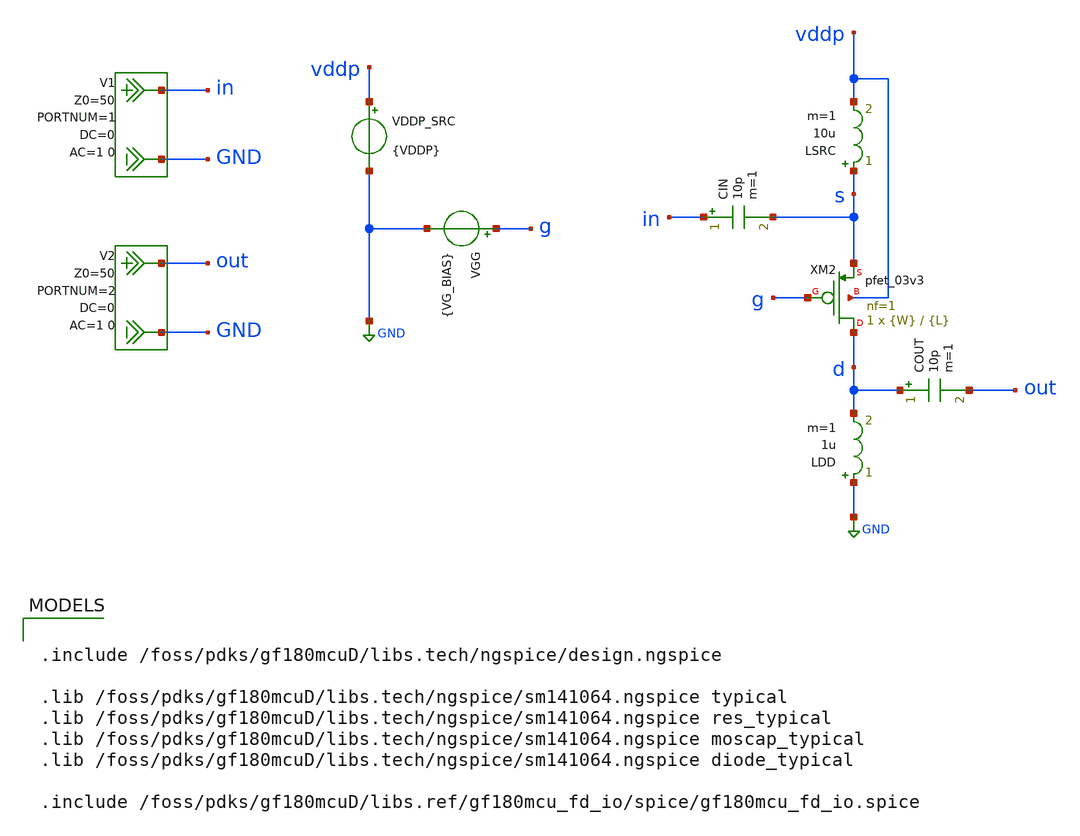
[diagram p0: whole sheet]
** sch_path: NFmin_Simulation/simulations/03v0/nfmin_jd_pmos_cg.sch
**.subckt nfmin_jd_pmos_cg
VGG g GND {VG_BIAS}
VDDP_SRC vddp GND {VDDP}
LDD GND d 1u m=1
COUT d out 10p m=1
CIN in s 10p m=1
XM2 d g s vddp pfet_03v3 L={L} W={W} nf=1 ad='int((nf+1)/2) * W/nf * 0.18u' as='int((nf+2)/2) * W/nf * 0.18u'
+ pd='2*int((nf+1)/2) * (W/nf + 0.18u)' ps='2*int((nf+2)/2) * (W/nf + 0.18u)' nrd='0.18u / W' nrs='0.18u / W'
+ sa=0 sb=0 sd=0 m=1
V1 in GND DC 0 AC 1 0 portnum 1 z0 50
V2 out GND DC 0 AC 1 0 portnum 2 z0 50
LSRC s vddp 10u m=1
**** begin user architecture code

.include /foss/pdks/gf180mcuD/libs.tech/ngspice/design.ngspice

.lib /foss/pdks/gf180mcuD/libs.tech/ngspice/sm141064.ngspice typical
.lib /foss/pdks/gf180mcuD/libs.tech/ngspice/sm141064.ngspice res_typical
.lib /foss/pdks/gf180mcuD/libs.tech/ngspice/sm141064.ngspice moscap_typical
.lib /foss/pdks/gf180mcuD/libs.tech/ngspice/sm141064.ngspice diode_typical

.include /foss/pdks/gf180mcuD/libs.ref/gf180mcu_fd_io/spice/gf180mcu_fd_io.spice



.option savecurrents

.param fnoicor=0
.param sw_stat_mismatch=0

.param VDDP=1.8
.param VSG_BIAS=0.7
.param VG_BIAS={VDDP-VSG_BIAS}

.param W=0.22e-6
.param L=0.28e-6

.control
  set noaskquit
  save all

  echo W_m L_m VSG ID_A JD_mA_per_um > pmos_cg_geom_jd_dense.txt
  echo W_m L_m VSG NFmin_dB NF_dB Rn SOpt_real SOpt_imag > pmos_cg_geom_nf_dense.txt

  foreach wval 0.22e-6 1e-6 5e-6 10e-6
    foreach lval 0.28e-6 0.36e-6 0.50e-6

      let vsg = 0.35

      while vsg le 1.2001

        alterparam W = $wval
        alterparam L = $lval
        alterparam VSG_BIAS = $&vsg
        reset

        op

        let idp_op = abs(i(vddp_src))
        let jd_p_op = 1e-3*idp_op/$wval

        echo $wval $lval $&vsg $&idp_op $&jd_p_op >> pmos_cg_geom_jd_dense.txt

        sp lin 1 2.4e9 2.4e9 1

        let nfmin_val = real(NFmin)
        let nf_val = real(NF)
        let rn_val = real(Rn)
        let sopt_re = real(SOpt)
        let sopt_im = imag(SOpt)

        echo $wval $lval $&vsg $&nfmin_val $&nf_val $&rn_val $&sopt_re $&sopt_im >>
+ pmos_cg_geom_nf_dense.txt

        let vsg = vsg + 0.005

      end
    end
  end

.endc



**** end user architecture code
**.ends
.GLOBAL GND
.end
